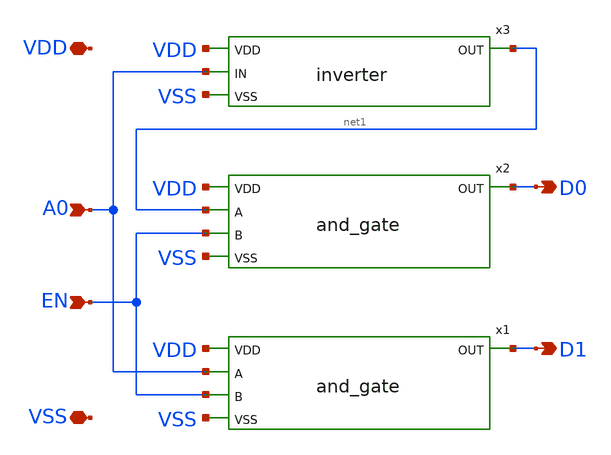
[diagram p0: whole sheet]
** sch_path: xschem/decoder_1bit.sch
**.subckt decoder_1bit VSS VDD A0 EN D0 D1
*.iopin VSS
*.iopin VDD
*.ipin A0
*.ipin EN
*.opin D0
*.opin D1
x1 VDD D1 A0 EN VSS and_gate
x2 VDD D0 net1 EN VSS and_gate
x3 VDD A0 net1 VSS inverter
**.ends
.end
